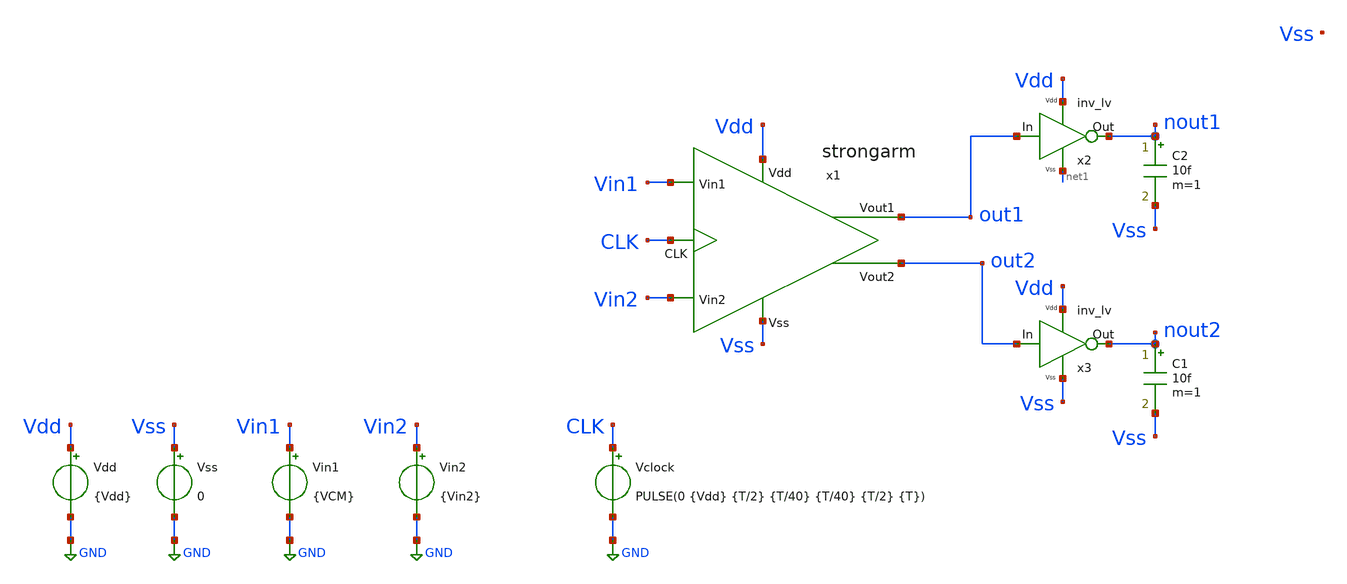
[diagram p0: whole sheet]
** sch_path: xschem/TB/TB_Tran_SA.sch
**.subckt TB_Tran_SA
Vdd Vdd GND {Vdd}
x1 out2 out1 Vdd Vss Vin2 Vin1 CLK strongarm
Vss Vss GND 0
C1 nout2 Vss 10f m=1
C2 nout1 Vss 10f m=1
Vin1 Vin1 GND {VCM}
Vin2 Vin2 GND {Vin2}
Vclock CLK GND PULSE(0 {Vdd} {T/2} {T/40} {T/40} {T/2} {T})
x2 out1 nout1 Vdd net1 inv_lv
x3 out2 nout2 Vdd Vss inv_lv
**** begin user architecture code


.param Vdd   = 1.8
.param VCM   = 0.9
.param Vstep = 1m
.param Vin2  = VCM-Vstep
.ic V(out1) = 0
.ic V(out2) = 0
.ic V(x1.common) = 0
.ic V(x1.P) = 0
.ic V(x1.Q) = 0





.lib cornerMOSlv.lib mos_tt




** TRANSISTORES NMOS

.param W12 = 1u
.param L12 = 0.2u
.param M12 = 1

.param W34 = 1u
.param L34 = 0.2u
.param M34 = 1

.param W56 = 1u
.param L56 = 0.2u
.param M56 = 1

.param W7  = 1u
.param L7  = 0.2u
.param M7  = 1

.param W89 = 1u
.param L89 = 0.2u
.param M89 = 1

.param Wab = 1u
.param Lab = 0.2u
.param Mab = 1





.param T = 10n
.control
*.param SimTime = 3*T + 100n
save all  @n.x1.xm1.nsg13_lv_nmos[gm]  @n.x1.xm1.nsg13_lv_nmos[ids]
  @n.x1.xm2.nsg13_lv_nmos[ids]  @n.x1.xm2.nsg13_lv_nmos[gm]
  @n.x1.xm3.nsg13_lv_nmos[ids]
  @n.x1.xm5.nsg13_lv_pmos[ids]  @n.x1.xm5.nsg13_lv_pmos[vds]  @n.x1.xm5.nsg13_lv_pmos[vgt]
  @n.x1.xm6.nsg13_lv_pmos[ids]  @n.x1.xm6.nsg13_lv_pmos[vds]
  @n.x1.xm7.nsg13_lv_nmos[ids]
  @n.x1.xm8.nsg13_lv_pmos[ids]
  @n.x1.xm10.nsg13_lv_pmos[vgt]


tran 10p 25n
let gm1  = @n.x1.xm1.nsg13_lv_nmos[gm]
let ids1 = @n.x1.xm1.nsg13_lv_nmos[ids]
let ids5 = @n.x1.xm5.nsg13_lv_pmos[ids]
let ids8 = @n.x1.xm8.nsg13_lv_pmos[ids]

meas tran Amp_t TRIG AT=15n TARG v(out1) VAL=0.9 CROSS=1
meas tran reg_t TRIG v(out1) VAL=0.9 CROSS=1 TARG v(out1) VAL=0.01 CROSS=1
meas tran Energy INTEG Pot from=15n to=25n
*plot v(x1.Q)
*plot v(x1.test)
*plot v(x1.P)
plot ids5 ids8
plot v(x1.vop) v(x1.voq)
.endc


**** end user architecture code
**.ends

* expanding   symbol:  ../sch/strongarm.sym # of pins=7
** sym_path: xschem/sch/strongarm.sym
** sch_path: xschem/sch/strongarm.sch
.subckt strongarm Vout2 Vout1 Vdd Vss Vin2 Vin1 CLK
*.opin Vout2
*.opin Vout1
*.ipin Vin1
*.ipin Vin2
*.ipin CLK
*.ipin Vss
*.ipin Vdd
XM1 common Vin1 P Vss sg13_lv_nmos w={W12} l={L12} ng=1 m={M12} mm_ok=1
XM2 common Vin2 Q Vss sg13_lv_nmos w={W12} l={L12} ng=1 m={M12} mm_ok=1
XM3 P Voq Vop Vss sg13_lv_nmos w={W34} l={L34} ng=1 m={M34} mm_ok=1
XM4 Q Vop Voq Vss sg13_lv_nmos w={W34} l={L34} ng=1 m={M34} mm_ok=1
XM6 Voq Vop Vdd Vdd sg13_lv_pmos w={W56} l={L56} ng=1 m={M56} mm_ok=1
XM5 Vop Voq Vdd Vdd sg13_lv_pmos w={W56} l={L56} ng=1 m={M56} mm_ok=1
XM7 Vss CLK common Vss sg13_lv_nmos w={W7} l={L7} ng=1 m={M7} mm_ok=1
XM8 P CLK Vdd Vdd sg13_lv_pmos w={W89} l={L89} ng=1 m={M89} mm_ok=1
XM9 Q CLK Vdd Vdd sg13_lv_pmos w={W89} l={L89} ng=1 m={M89} mm_ok=1
XM11 Voq CLK Vdd Vdd sg13_lv_pmos w={Wab} l={Lab} ng=1 m={Wab} mm_ok=1
XM10 Vop CLK Vdd Vdd sg13_lv_pmos w={Wab} l={Lab} ng=1 m={Wab} mm_ok=1
.ends


* expanding   symbol:  ../sch/inv_lv.sym # of pins=4
** sym_path: xschem/sch/inv_lv.sym
** sch_path: xschem/sch/inv_lv.sch
.subckt inv_lv Vin Vout Vdd Vss
*.ipin Vdd
*.ipin Vss
*.ipin Vin
*.opin Vout
XM1 Vss Vin Vout Vss sg13_lv_nmos w=1u l=0.13u ng=1 m=1 mm_ok=1
XM2 Vout Vin Vdd Vdd sg13_lv_pmos w=2.3u l=0.13u ng=1 m=1 mm_ok=1
.ends

.GLOBAL GND
.end
